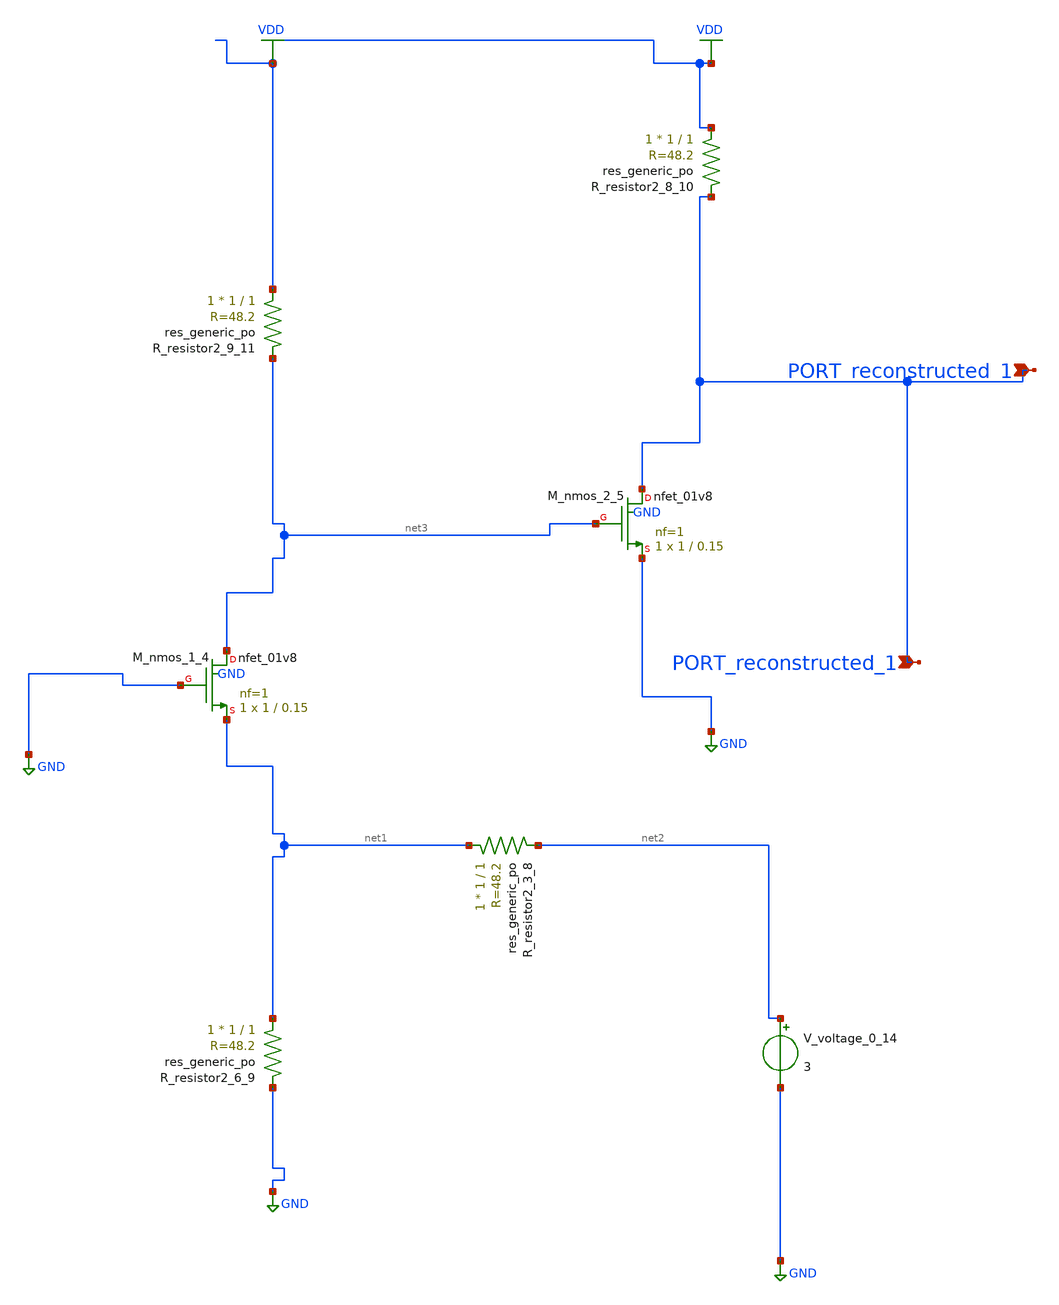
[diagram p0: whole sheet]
** sch_path: schematics/AMSNet/596.sch
**.subckt 596 PORT_reconstructed_1 PORT_reconstructed_1
*.ipin PORT_reconstructed_1
*.ipin PORT_reconstructed_1
XM_nmos_1_4 net3 GND net1 GND sky130_fd_pr__nfet_01v8 L=0.15 W=1 nf=1 ad='int((1 + 1)/2) * 1 / 1 * 0.29'
+ as='int((1 + 2)/2) * 1 / 1 * 0.29' pd='2*int((1 + 1)/2) * (1 / 1 + 0.29)' ps='2*int((1 + 2)/2) * (1 / 1 + 0.29)'
+ nrd='0.29 / 1 ' nrs='0.29 / 1 ' sa=0 sb=0 sd=0 mult=1 m=1
XM_nmos_2_5 PORT_reconstructed_1 net3 GND GND sky130_fd_pr__nfet_01v8 L=0.15 W=1 nf=1 ad='int((1 + 1)/2) * 1 / 1 * 0.29'
+ as='int((1 + 2)/2) * 1 / 1 * 0.29' pd='2*int((1 + 1)/2) * (1 / 1 + 0.29)' ps='2*int((1 + 2)/2) * (1 / 1 + 0.29)'
+ nrd='0.29 / 1 ' nrs='0.29 / 1 ' sa=0 sb=0 sd=0 mult=1 m=1
XR_resistor2_3_8 net1 net2 sky130_fd_pr__res_generic_po W=1 L=1 m=1
XR_resistor2_6_9 net1 GND sky130_fd_pr__res_generic_po W=1 L=1 m=1
XR_resistor2_8_10 VDD PORT_reconstructed_1 sky130_fd_pr__res_generic_po W=1 L=1 m=1
XR_resistor2_9_11 VDD net3 sky130_fd_pr__res_generic_po W=1 L=1 m=1
V_voltage_0_14 net2 GND 3
**.ends
.GLOBAL GND
.GLOBAL VDD
.end
